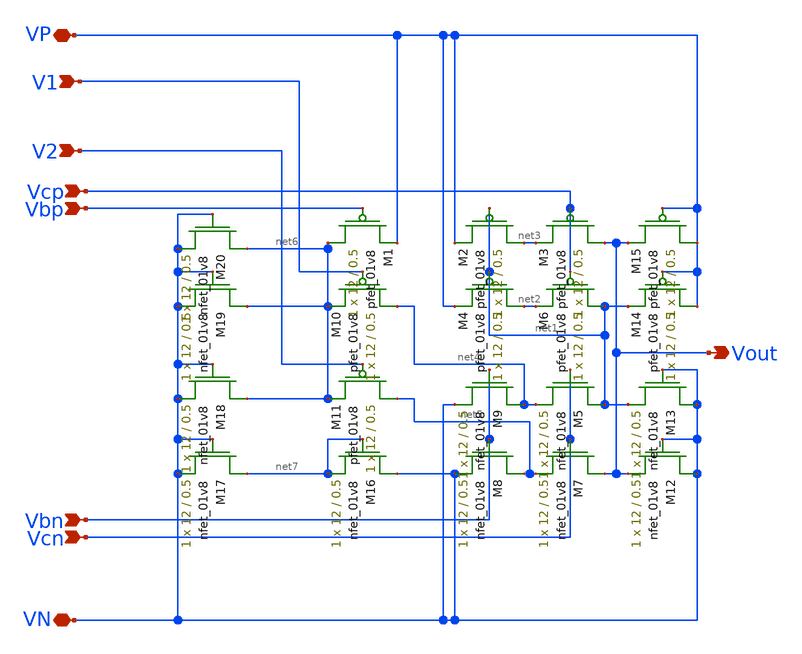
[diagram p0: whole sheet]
** sch_path: MiniProject3-Cascode/XSCHEM/fcascodediffamp.sch
**.subckt fcascodediffamp VP VN V1 V2 Vbp Vcp Vcn Vbn Vout
*.iopin VP
*.iopin VN
*.ipin V1
*.ipin V2
*.ipin Vbp
*.ipin Vcp
*.ipin Vcn
*.ipin Vbn
*.opin Vout
XM5 net1 Vcn net4 GND sky130_fd_pr__nfet_01v8 L=0.5 W=12 nf=1 ad='int((nf+1)/2) * W/nf * 0.29' as='int((nf+2)/2) * W/nf * 0.29'
+ pd='2*int((nf+1)/2) * (W/nf + 0.29)' ps='2*int((nf+2)/2) * (W/nf + 0.29)' nrd='0.29 / W' nrs='0.29 / W'
+ sa=0 sb=0 sd=0 mult=1 m=1
XM2 net3 net1 VP VDD sky130_fd_pr__pfet_01v8 L=0.5 W=12 nf=1 ad='int((nf+1)/2) * W/nf * 0.29' as='int((nf+2)/2) * W/nf * 0.29'
+ pd='2*int((nf+1)/2) * (W/nf + 0.29)' ps='2*int((nf+2)/2) * (W/nf + 0.29)' nrd='0.29 / W' nrs='0.29 / W'
+ sa=0 sb=0 sd=0 mult=1 m=1
XM3 Vout Vcp net3 VDD sky130_fd_pr__pfet_01v8 L=0.5 W=12 nf=1 ad='int((nf+1)/2) * W/nf * 0.29' as='int((nf+2)/2) * W/nf * 0.29'
+ pd='2*int((nf+1)/2) * (W/nf + 0.29)' ps='2*int((nf+2)/2) * (W/nf + 0.29)' nrd='0.29 / W' nrs='0.29 / W'
+ sa=0 sb=0 sd=0 mult=1 m=1
XM4 net2 net1 VP VDD sky130_fd_pr__pfet_01v8 L=0.5 W=12 nf=1 ad='int((nf+1)/2) * W/nf * 0.29' as='int((nf+2)/2) * W/nf * 0.29'
+ pd='2*int((nf+1)/2) * (W/nf + 0.29)' ps='2*int((nf+2)/2) * (W/nf + 0.29)' nrd='0.29 / W' nrs='0.29 / W'
+ sa=0 sb=0 sd=0 mult=1 m=1
XM6 net1 Vcp net2 VDD sky130_fd_pr__pfet_01v8 L=0.5 W=12 nf=1 ad='int((nf+1)/2) * W/nf * 0.29' as='int((nf+2)/2) * W/nf * 0.29'
+ pd='2*int((nf+1)/2) * (W/nf + 0.29)' ps='2*int((nf+2)/2) * (W/nf + 0.29)' nrd='0.29 / W' nrs='0.29 / W'
+ sa=0 sb=0 sd=0 mult=1 m=1
XM7 Vout Vcn net5 GND sky130_fd_pr__nfet_01v8 L=0.5 W=12 nf=1 ad='int((nf+1)/2) * W/nf * 0.29' as='int((nf+2)/2) * W/nf * 0.29'
+ pd='2*int((nf+1)/2) * (W/nf + 0.29)' ps='2*int((nf+2)/2) * (W/nf + 0.29)' nrd='0.29 / W' nrs='0.29 / W'
+ sa=0 sb=0 sd=0 mult=1 m=1
XM8 net5 Vbn VN GND sky130_fd_pr__nfet_01v8 L=0.5 W=12 nf=1 ad='int((nf+1)/2) * W/nf * 0.29' as='int((nf+2)/2) * W/nf * 0.29'
+ pd='2*int((nf+1)/2) * (W/nf + 0.29)' ps='2*int((nf+2)/2) * (W/nf + 0.29)' nrd='0.29 / W' nrs='0.29 / W'
+ sa=0 sb=0 sd=0 mult=1 m=1
XM9 net4 Vbn VN GND sky130_fd_pr__nfet_01v8 L=0.5 W=12 nf=1 ad='int((nf+1)/2) * W/nf * 0.29' as='int((nf+2)/2) * W/nf * 0.29'
+ pd='2*int((nf+1)/2) * (W/nf + 0.29)' ps='2*int((nf+2)/2) * (W/nf + 0.29)' nrd='0.29 / W' nrs='0.29 / W'
+ sa=0 sb=0 sd=0 mult=1 m=1
XM12 VN VN Vout GND sky130_fd_pr__nfet_01v8 L=0.5 W=12 nf=1 ad='int((nf+1)/2) * W/nf * 0.29' as='int((nf+2)/2) * W/nf * 0.29'
+ pd='2*int((nf+1)/2) * (W/nf + 0.29)' ps='2*int((nf+2)/2) * (W/nf + 0.29)' nrd='0.29 / W' nrs='0.29 / W'
+ sa=0 sb=0 sd=0 mult=1 m=1
XM13 VN VN net1 GND sky130_fd_pr__nfet_01v8 L=0.5 W=12 nf=1 ad='int((nf+1)/2) * W/nf * 0.29' as='int((nf+2)/2) * W/nf * 0.29'
+ pd='2*int((nf+1)/2) * (W/nf + 0.29)' ps='2*int((nf+2)/2) * (W/nf + 0.29)' nrd='0.29 / W' nrs='0.29 / W'
+ sa=0 sb=0 sd=0 mult=1 m=1
XM14 VP VP net1 VDD sky130_fd_pr__pfet_01v8 L=0.5 W=12 nf=1 ad='int((nf+1)/2) * W/nf * 0.29' as='int((nf+2)/2) * W/nf * 0.29'
+ pd='2*int((nf+1)/2) * (W/nf + 0.29)' ps='2*int((nf+2)/2) * (W/nf + 0.29)' nrd='0.29 / W' nrs='0.29 / W'
+ sa=0 sb=0 sd=0 mult=1 m=1
XM15 VP VP Vout VDD sky130_fd_pr__pfet_01v8 L=0.5 W=12 nf=1 ad='int((nf+1)/2) * W/nf * 0.29' as='int((nf+2)/2) * W/nf * 0.29'
+ pd='2*int((nf+1)/2) * (W/nf + 0.29)' ps='2*int((nf+2)/2) * (W/nf + 0.29)' nrd='0.29 / W' nrs='0.29 / W'
+ sa=0 sb=0 sd=0 mult=1 m=1
XM1 net6 Vbp VP VDD sky130_fd_pr__pfet_01v8 L=0.5 W=12 nf=1 ad='int((nf+1)/2) * W/nf * 0.29' as='int((nf+2)/2) * W/nf * 0.29'
+ pd='2*int((nf+1)/2) * (W/nf + 0.29)' ps='2*int((nf+2)/2) * (W/nf + 0.29)' nrd='0.29 / W' nrs='0.29 / W'
+ sa=0 sb=0 sd=0 mult=1 m=1
XM10 net4 V1 net6 VDD sky130_fd_pr__pfet_01v8 L=0.5 W=12 nf=1 ad='int((nf+1)/2) * W/nf * 0.29' as='int((nf+2)/2) * W/nf * 0.29'
+ pd='2*int((nf+1)/2) * (W/nf + 0.29)' ps='2*int((nf+2)/2) * (W/nf + 0.29)' nrd='0.29 / W' nrs='0.29 / W'
+ sa=0 sb=0 sd=0 mult=1 m=1
XM11 net5 V2 net6 VDD sky130_fd_pr__pfet_01v8 L=0.5 W=12 nf=1 ad='int((nf+1)/2) * W/nf * 0.29' as='int((nf+2)/2) * W/nf * 0.29'
+ pd='2*int((nf+1)/2) * (W/nf + 0.29)' ps='2*int((nf+2)/2) * (W/nf + 0.29)' nrd='0.29 / W' nrs='0.29 / W'
+ sa=0 sb=0 sd=0 mult=1 m=1
XM16 VN net7 net7 GND sky130_fd_pr__nfet_01v8 L=0.5 W=12 nf=1 ad='int((nf+1)/2) * W/nf * 0.29' as='int((nf+2)/2) * W/nf * 0.29'
+ pd='2*int((nf+1)/2) * (W/nf + 0.29)' ps='2*int((nf+2)/2) * (W/nf + 0.29)' nrd='0.29 / W' nrs='0.29 / W'
+ sa=0 sb=0 sd=0 mult=1 m=1
XM17 net7 VN VN GND sky130_fd_pr__nfet_01v8 L=0.5 W=12 nf=1 ad='int((nf+1)/2) * W/nf * 0.29' as='int((nf+2)/2) * W/nf * 0.29'
+ pd='2*int((nf+1)/2) * (W/nf + 0.29)' ps='2*int((nf+2)/2) * (W/nf + 0.29)' nrd='0.29 / W' nrs='0.29 / W'
+ sa=0 sb=0 sd=0 mult=1 m=1
XM18 net6 VN VN GND sky130_fd_pr__nfet_01v8 L=0.5 W=12 nf=1 ad='int((nf+1)/2) * W/nf * 0.29' as='int((nf+2)/2) * W/nf * 0.29'
+ pd='2*int((nf+1)/2) * (W/nf + 0.29)' ps='2*int((nf+2)/2) * (W/nf + 0.29)' nrd='0.29 / W' nrs='0.29 / W'
+ sa=0 sb=0 sd=0 mult=1 m=1
XM19 net6 VN VN GND sky130_fd_pr__nfet_01v8 L=0.5 W=12 nf=1 ad='int((nf+1)/2) * W/nf * 0.29' as='int((nf+2)/2) * W/nf * 0.29'
+ pd='2*int((nf+1)/2) * (W/nf + 0.29)' ps='2*int((nf+2)/2) * (W/nf + 0.29)' nrd='0.29 / W' nrs='0.29 / W'
+ sa=0 sb=0 sd=0 mult=1 m=1
XM20 net6 VN VN GND sky130_fd_pr__nfet_01v8 L=0.5 W=12 nf=1 ad='int((nf+1)/2) * W/nf * 0.29' as='int((nf+2)/2) * W/nf * 0.29'
+ pd='2*int((nf+1)/2) * (W/nf + 0.29)' ps='2*int((nf+2)/2) * (W/nf + 0.29)' nrd='0.29 / W' nrs='0.29 / W'
+ sa=0 sb=0 sd=0 mult=1 m=1
**.ends
.end
